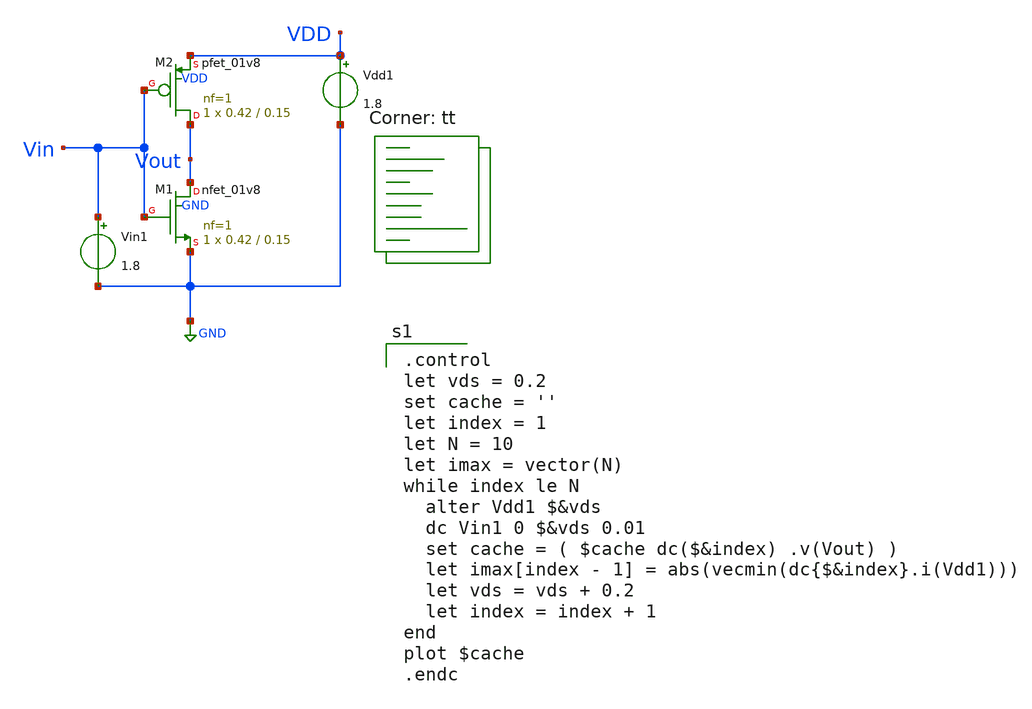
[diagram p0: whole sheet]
** sch_path: tut2/expt2_1/expt2_1.sch
**.subckt expt2_1
XM1 Vout Vin GND GND sky130_fd_pr__nfet_01v8 L=0.15 W=0.42 nf=1 ad='int((nf+1)/2) * W/nf * 0.29' as='int((nf+2)/2) * W/nf * 0.29'
+ pd='2*int((nf+1)/2) * (W/nf + 0.29)' ps='2*int((nf+2)/2) * (W/nf + 0.29)' nrd='0.29 / W' nrs='0.29 / W'
+ sa=0 sb=0 sd=0 mult=1 m=1
Vin1 Vin GND 1.8
XM2 Vout Vin VDD VDD sky130_fd_pr__pfet_01v8 L=0.15 W=0.42 nf=1 ad='int((nf+1)/2) * W/nf * 0.29' as='int((nf+2)/2) * W/nf * 0.29'
+ pd='2*int((nf+1)/2) * (W/nf + 0.29)' ps='2*int((nf+2)/2) * (W/nf + 0.29)' nrd='0.29 / W' nrs='0.29 / W'
+ sa=0 sb=0 sd=0 mult=1 m=1
Vdd1 VDD GND 1.8
**** begin user architecture code
.lib $::SKYWATER_MODELS/sky130.lib.spice tt

.control
let vds = 0.2
set cache = ''
let index = 1
let N = 10
let imax = vector(N)
while index le N
  alter Vdd1 $&vds
  dc Vin1 0 $&vds 0.01
  set cache = ( $cache dc($&index) .v(Vout) )
  let imax[index - 1] = abs(vecmin(dc{$&index}.i(Vdd1)))
  let vds = vds + 0.2
  let index = index + 1
end
plot $cache
.endc

**** end user architecture code
**.ends
.GLOBAL GND
.end
